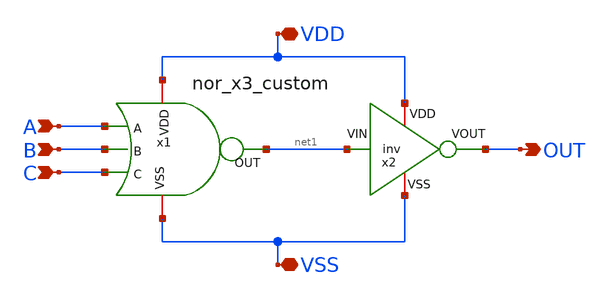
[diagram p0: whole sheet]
** sch_path: Custom_std_cells/or_x3_custom.sch
**.subckt or_x3_custom VDD VSS OUT A B C
*.iopin VDD
*.iopin VSS
*.opin OUT
*.ipin A
*.ipin B
*.ipin C
x1 VDD A B C net1 VSS nor_x3_custom
x2 VDD OUT net1 VSS inv
**.ends

* expanding   symbol:  /foss/designs/PhaseInterpolator/Custom_std_cells/nor_x3_custom.sym # of
*+ pins=6
** sym_path: /foss/designs/PhaseInterpolator/Custom_std_cells/nor_x3_custom.sym
** sch_path: /foss/designs/PhaseInterpolator/Custom_std_cells/nor_x3_custom.sch
.subckt nor_x3_custom VDD A B C OUT VSS
*.iopin VDD
*.iopin VSS
*.ipin B
*.ipin C
*.opin OUT
*.ipin A
XM1 OUT A VSS VSS sg13_lv_nmos w=0.15u l=0.13u ng=1 m=1 mm_ok=1
XM2 OUT C net1 VDD sg13_lv_pmos w=0.45u l=0.13u ng=1 m=1 mm_ok=1
XM3 OUT B VSS VSS sg13_lv_nmos w=0.15u l=0.13u ng=1 m=1 mm_ok=1
XM4 net1 B net2 VDD sg13_lv_pmos w=0.45u l=0.13u ng=1 m=1 mm_ok=1
XM5 net2 A VDD VDD sg13_lv_pmos w=0.45u l=0.13u ng=1 m=1 mm_ok=1
XM6 OUT C VSS VSS sg13_lv_nmos w=0.15u l=0.13u ng=1 m=1 mm_ok=1
.ends

.end
